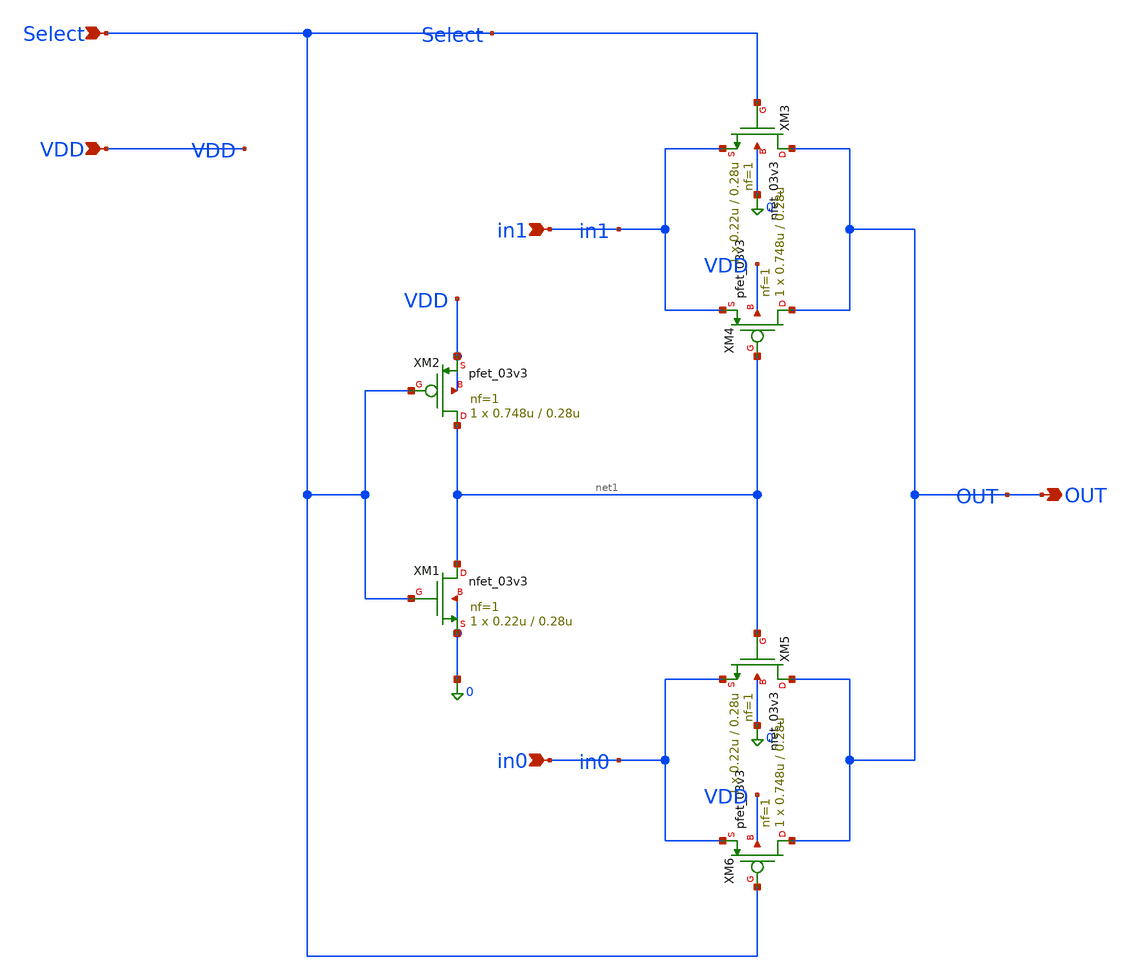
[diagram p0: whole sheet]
** sch_path: Design_Files/IC Design/Schematic/SAR_ADC_BLOCKS/MUX/MUX.sch
**.subckt MUX Select OUT in1 in0 VDD
*.ipin Select
*.opin OUT
*.ipin in1
*.ipin in0
*.ipin VDD
XM1 net1 Select 0 0 nfet_03v3 L=0.28u W=0.22u nf=1 ad='int((nf+1)/2) * W/nf * 0.18u' as='int((nf+2)/2) * W/nf * 0.18u'
+ pd='2*int((nf+1)/2) * (W/nf + 0.18u)' ps='2*int((nf+2)/2) * (W/nf + 0.18u)' nrd='0.18u / W' nrs='0.18u / W'
+ sa=0 sb=0 sd=0 m=1
XM2 net1 Select VDD VDD pfet_03v3 L=0.28u W=0.748u nf=1 ad='int((nf+1)/2) * W/nf * 0.18u' as='int((nf+2)/2) * W/nf * 0.18u'
+ pd='2*int((nf+1)/2) * (W/nf + 0.18u)' ps='2*int((nf+2)/2) * (W/nf + 0.18u)' nrd='0.18u / W' nrs='0.18u / W'
+ sa=0 sb=0 sd=0 m=1
XM3 OUT Select in1 0 nfet_03v3 L=0.28u W=0.22u nf=1 ad='int((nf+1)/2) * W/nf * 0.18u' as='int((nf+2)/2) * W/nf * 0.18u'
+ pd='2*int((nf+1)/2) * (W/nf + 0.18u)' ps='2*int((nf+2)/2) * (W/nf + 0.18u)' nrd='0.18u / W' nrs='0.18u / W'
+ sa=0 sb=0 sd=0 m=1
XM4 OUT net1 in1 VDD pfet_03v3 L=0.28u W=0.748u nf=1 ad='int((nf+1)/2) * W/nf * 0.18u' as='int((nf+2)/2) * W/nf * 0.18u'
+ pd='2*int((nf+1)/2) * (W/nf + 0.18u)' ps='2*int((nf+2)/2) * (W/nf + 0.18u)' nrd='0.18u / W' nrs='0.18u / W'
+ sa=0 sb=0 sd=0 m=1
XM5 OUT net1 in0 0 nfet_03v3 L=0.28u W=0.22u nf=1 ad='int((nf+1)/2) * W/nf * 0.18u' as='int((nf+2)/2) * W/nf * 0.18u'
+ pd='2*int((nf+1)/2) * (W/nf + 0.18u)' ps='2*int((nf+2)/2) * (W/nf + 0.18u)' nrd='0.18u / W' nrs='0.18u / W'
+ sa=0 sb=0 sd=0 m=1
XM6 OUT Select in0 VDD pfet_03v3 L=0.28u W=0.748u nf=1 ad='int((nf+1)/2) * W/nf * 0.18u' as='int((nf+2)/2) * W/nf * 0.18u'
+ pd='2*int((nf+1)/2) * (W/nf + 0.18u)' ps='2*int((nf+2)/2) * (W/nf + 0.18u)' nrd='0.18u / W' nrs='0.18u / W'
+ sa=0 sb=0 sd=0 m=1
**.ends
.end
